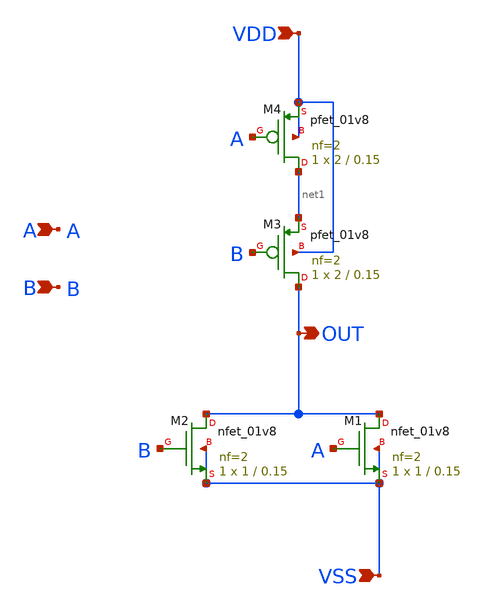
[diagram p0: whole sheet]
** sch_path: design/LELO_SVOD_SKY130A/LELO_NOR.sch
**.subckt LELO_NOR VDD VSS OUT A B
*.ipin VDD
*.ipin VSS
*.opin OUT
*.ipin A
*.ipin B
XM2 OUT B VSS VSS sky130_fd_pr__nfet_01v8 L=0.15 W=1 nf=2 ad='int((2 + 1)/2) * 1 / 2 * 0.29' as='int((2 + 2)/2) * 1 / 2 * 0.29'
+ pd='2*int((2 + 1)/2) * (1 / 2 + 0.29)' ps='2*int((2 + 2)/2) * (1 / 2 + 0.29)' nrd='0.29 / 1 ' nrs='0.29 / 1 '
+ sa=0 sb=0 sd=0 mult=1 m=1
XM3 OUT B net1 VDD sky130_fd_pr__pfet_01v8 L=0.15 W=2 nf=2 ad='int((2 + 1)/2) * 2 / 2 * 0.29' as='int((2 + 2)/2) * 2 / 2 * 0.29'
+ pd='2*int((2 + 1)/2) * (2 / 2 + 0.29)' ps='2*int((2 + 2)/2) * (2 / 2 + 0.29)' nrd='0.29 / 2 ' nrs='0.29 / 2 '
+ sa=0 sb=0 sd=0 mult=1 m=1
XM1 OUT A VSS VSS sky130_fd_pr__nfet_01v8 L=0.15 W=1 nf=2 ad='int((2 + 1)/2) * 1 / 2 * 0.29' as='int((2 + 2)/2) * 1 / 2 * 0.29'
+ pd='2*int((2 + 1)/2) * (1 / 2 + 0.29)' ps='2*int((2 + 2)/2) * (1 / 2 + 0.29)' nrd='0.29 / 1 ' nrs='0.29 / 1 '
+ sa=0 sb=0 sd=0 mult=1 m=1
XM4 net1 A VDD VDD sky130_fd_pr__pfet_01v8 L=0.15 W=2 nf=2 ad='int((2 + 1)/2) * 2 / 2 * 0.29' as='int((2 + 2)/2) * 2 / 2 * 0.29'
+ pd='2*int((2 + 1)/2) * (2 / 2 + 0.29)' ps='2*int((2 + 2)/2) * (2 / 2 + 0.29)' nrd='0.29 / 2 ' nrs='0.29 / 2 '
+ sa=0 sb=0 sd=0 mult=1 m=1
**.ends
.end
